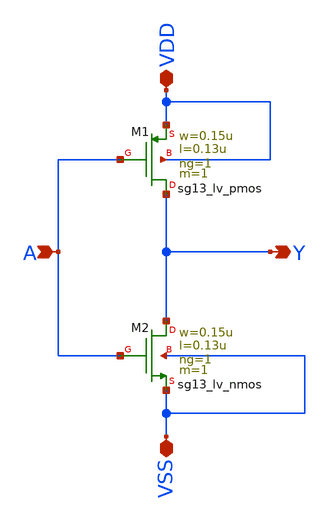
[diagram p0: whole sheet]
** sch_path: inverter.sch
**.subckt inverter A VDD VSS Y
*.ipin A
*.iopin VDD
*.iopin VSS
*.opin Y
XM1 Y A VDD VDD sg13_lv_pmos w=0.15u l=0.13u ng=1 m=1 mm_ok=1
XM2 Y A VSS VSS sg13_lv_nmos w=0.15u l=0.13u ng=1 m=1 mm_ok=1
**.ends
.end
